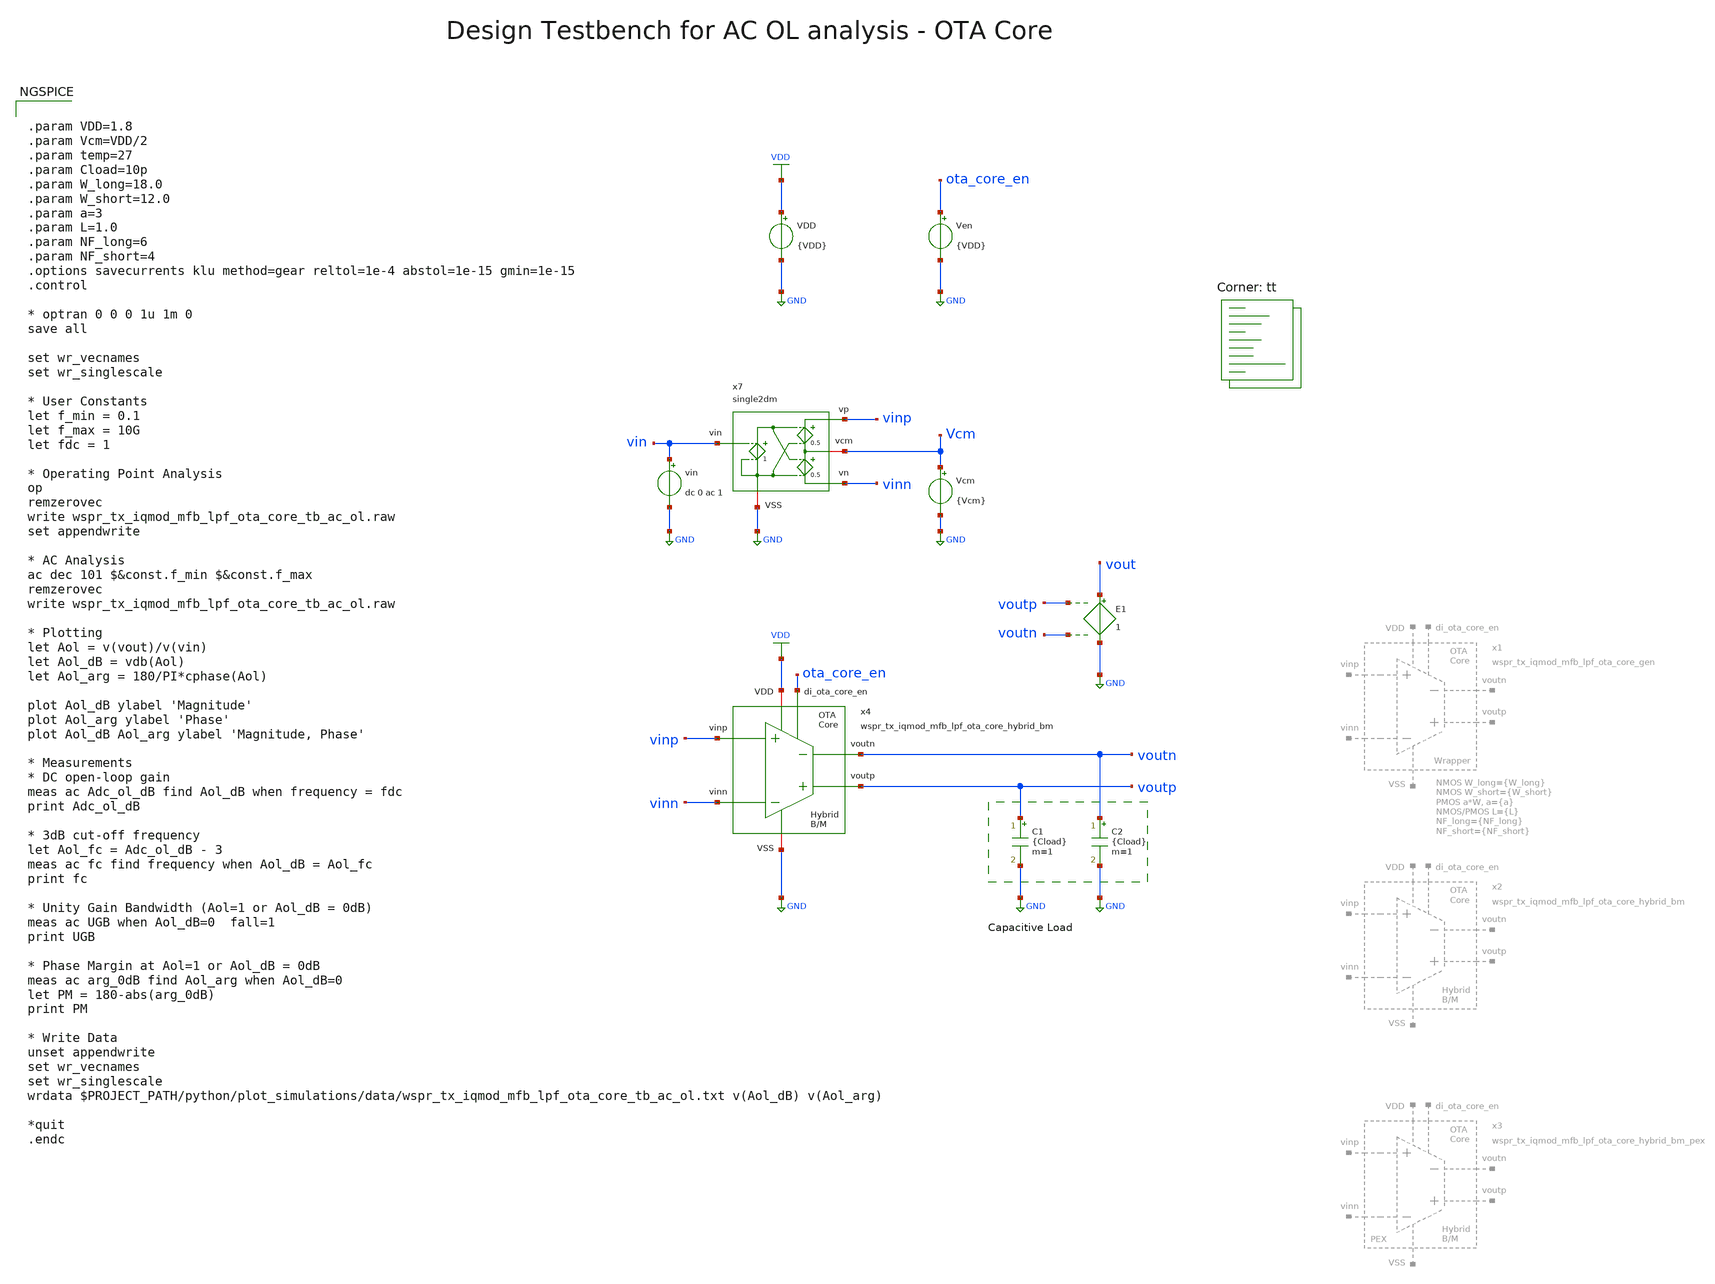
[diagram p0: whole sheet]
** sch_path: sky130/macros/iqmod/testbenches/wspr_tx_iqmod_mfb_lpf_ota_core_tb_ac_ol.sch
**.subckt wspr_tx_iqmod_mfb_lpf_ota_core_tb_ac_ol
VDD VDD GND {VDD}
C1 voutp GND {Cload} m=1
C2 voutn GND {Cload} m=1
Ven ota_core_en GND {VDD}
E1 vout GND voutp voutn 1
vin vin GND dc 0 ac 1
x4 ota_core_en voutp voutn vinn vinp VDD GND wspr_tx_iqmod_mfb_lpf_ota_core_hybrid_bm
x7 vinp vin Vcm GND vinn single2dm
Vcm Vcm GND {Vcm}
**** begin user architecture code


.param VDD=1.8
.param Vcm=VDD/2
.param temp=27
.param Cload=10p
.param W_long=18.0
.param W_short=12.0
.param a=3
.param L=1.0
.param NF_long=6
.param NF_short=4
.options savecurrents klu method=gear reltol=1e-4 abstol=1e-15 gmin=1e-15
.control

* optran 0 0 0 1u 1m 0
save all

set wr_vecnames
set wr_singlescale

* User Constants
let f_min = 0.1
let f_max = 10G
let fdc = 1

* Operating Point Analysis
op
remzerovec
write wspr_tx_iqmod_mfb_lpf_ota_core_tb_ac_ol.raw
set appendwrite

* AC Analysis
ac dec 101 $&const.f_min $&const.f_max
remzerovec
write wspr_tx_iqmod_mfb_lpf_ota_core_tb_ac_ol.raw

* Plotting
let Aol = v(vout)/v(vin)
let Aol_dB = vdb(Aol)
let Aol_arg = 180/PI*cphase(Aol)

plot Aol_dB ylabel 'Magnitude'
plot Aol_arg ylabel 'Phase'
plot Aol_dB Aol_arg ylabel 'Magnitude, Phase'

* Measurements
* DC open-loop gain
meas ac Adc_ol_dB find Aol_dB when frequency = fdc
print Adc_ol_dB

* 3dB cut-off frequency
let Aol_fc = Adc_ol_dB - 3
meas ac fc find frequency when Aol_dB = Aol_fc
print fc

* Unity Gain Bandwidth (Aol=1 or Aol_dB = 0dB)
meas ac UGB when Aol_dB=0  fall=1
print UGB

* Phase Margin at Aol=1 or Aol_dB = 0dB
meas ac arg_0dB find Aol_arg when Aol_dB=0
let PM = 180-abs(arg_0dB)
print PM

* Write Data
unset appendwrite
set wr_vecnames
set wr_singlescale
wrdata $PROJECT_PATH/python/plot_simulations/data/wspr_tx_iqmod_mfb_lpf_ota_core_tb_ac_ol.txt
+ v(Aol_dB) v(Aol_arg)

*quit
.endc


.lib $::SKYWATER_MODELS/sky130.lib.spice tt
**** end user architecture code
**.ends
.GLOBAL GND
.GLOBAL VDD
.end
